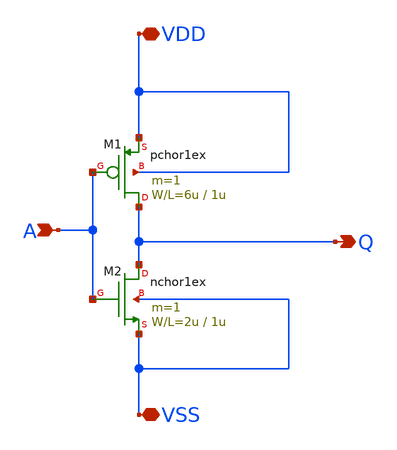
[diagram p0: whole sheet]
** sch_path: member_project/kensukeyama/kensuke/inverter.sch
**.subckt inverter Q VDD VSS A
*.opin Q
*.iopin VDD
*.iopin VSS
*.ipin A
M1 Q A VDD VDD pchor1ex L=1u W=6u m=1
M2 Q A VSS VSS nchor1ex L=1u W=2u m=1
**.ends
.end
